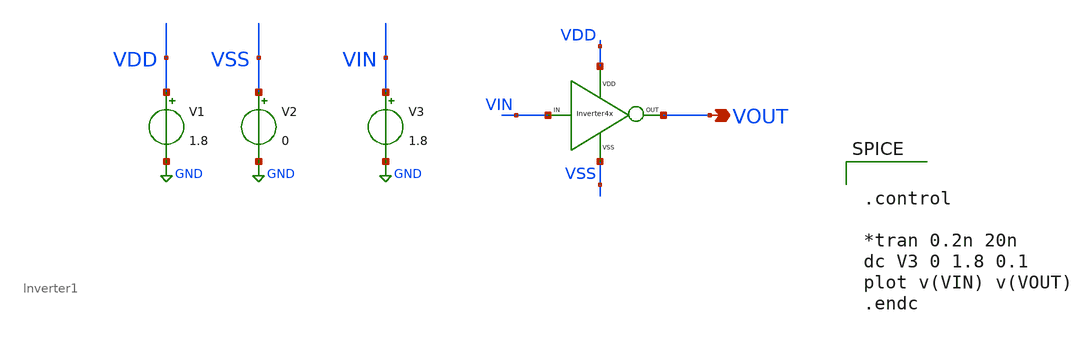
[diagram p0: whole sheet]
** sch_path: xschem/DC_DC_Converter_xschem/OTHERS/DC_DC_Converter_3/Inverter_1/Inverter1_TB.sch
**.subckt Inverter1_TB VOUT
*.opin VOUT
V1 VDD GND 1.8
V2 VSS GND 0
V3 VIN GND 1.8
X1 VIN VOUT VDD VSS Inverter1
**** begin user architecture code


.control

*tran 0.2n 20n
dc V3 0 1.8 0.1
plot v(VIN) v(VOUT)
.endc



** opencircuitdesign pdks install
.lib $::SKYWATER_MODELS/sky130.lib.spice tt


**** end user architecture code
**.ends
.GLOBAL GND
.end
